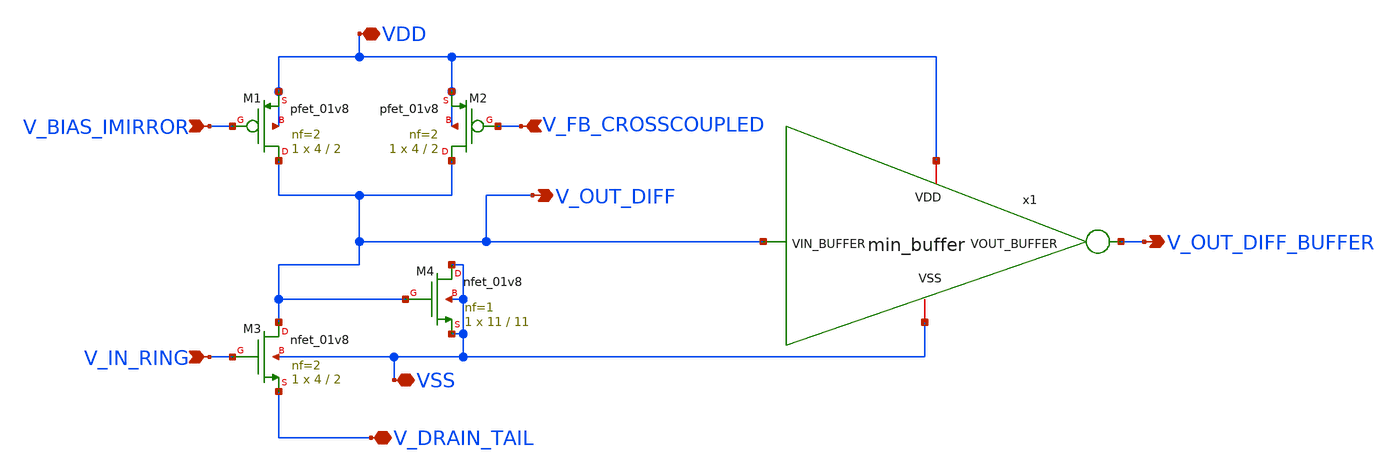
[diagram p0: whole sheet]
** sch_path: xschem/diff_stage_half.sch
**.subckt diff_stage_half V_BIAS_IMIRROR V_FB_CROSSCOUPLED V_IN_RING V_OUT_DIFF VDD VSS
*+ V_OUT_DIFF_BUFFER V_DRAIN_TAIL
*.ipin V_BIAS_IMIRROR
*.ipin V_FB_CROSSCOUPLED
*.ipin V_IN_RING
*.opin V_OUT_DIFF
*.iopin VDD
*.iopin VSS
*.opin V_OUT_DIFF_BUFFER
*.iopin V_DRAIN_TAIL
XM1 V_OUT_DIFF V_BIAS_IMIRROR VDD VDD sky130_fd_pr__pfet_01v8 L=2 W=4 nf=2 ad='int((nf+1)/2) * W/nf * 0.29'
+ as='int((nf+2)/2) * W/nf * 0.29' pd='2*int((nf+1)/2) * (W/nf + 0.29)' ps='2*int((nf+2)/2) * (W/nf + 0.29)'
+ nrd='0.29 / W' nrs='0.29 / W' sa=0 sb=0 sd=0 mult=1 m=1
XM2 V_OUT_DIFF V_FB_CROSSCOUPLED VDD VDD sky130_fd_pr__pfet_01v8 L=2 W=4 nf=2 ad='int((nf+1)/2) * W/nf * 0.29'
+ as='int((nf+2)/2) * W/nf * 0.29' pd='2*int((nf+1)/2) * (W/nf + 0.29)' ps='2*int((nf+2)/2) * (W/nf + 0.29)'
+ nrd='0.29 / W' nrs='0.29 / W' sa=0 sb=0 sd=0 mult=1 m=1
XM3 V_OUT_DIFF V_IN_RING V_DRAIN_TAIL VSS sky130_fd_pr__nfet_01v8 L=2 W=4 nf=2 ad='int((nf+1)/2) * W/nf * 0.29'
+ as='int((nf+2)/2) * W/nf * 0.29' pd='2*int((nf+1)/2) * (W/nf + 0.29)' ps='2*int((nf+2)/2) * (W/nf + 0.29)'
+ nrd='0.29 / W' nrs='0.29 / W' sa=0 sb=0 sd=0 mult=1 m=1
XM4 VSS V_OUT_DIFF VSS VSS sky130_fd_pr__nfet_01v8 L=11 W=11 nf=1 ad='int((nf+1)/2) * W/nf * 0.29' as='int((nf+2)/2) * W/nf * 0.29'
+ pd='2*int((nf+1)/2) * (W/nf + 0.29)' ps='2*int((nf+2)/2) * (W/nf + 0.29)' nrd='0.29 / W' nrs='0.29 / W'
+ sa=0 sb=0 sd=0 mult=1 m=1
x1 VDD VSS V_OUT_DIFF_BUFFER V_OUT_DIFF min_buffer
**.ends

* expanding   symbol:  min_buffer.sym # of pins=4
** sym_path: xschem/min_buffer.sym
** sch_path: xschem/min_buffer.sch
.subckt min_buffer VDD VSS VOUT_BUFFER VIN_BUFFER
*.ipin VIN_BUFFER
*.opin VOUT_BUFFER
*.iopin VDD
*.iopin VSS
x1 VDD VSS VOUT_BUFFER INT_BUFFER min_inv
x2 VDD VSS INT_BUFFER VIN_BUFFER min_inv
.ends


* expanding   symbol:  min_inv.sym # of pins=4
** sym_path: xschem/min_inv.sym
** sch_path: xschem/min_inv.sch
.subckt min_inv VDD VSS VOUT_INV VIN_INV
*.iopin VDD
*.iopin VSS
*.ipin VIN_INV
*.opin VOUT_INV
XM2 VOUT_INV VIN_INV VSS VSS sky130_fd_pr__nfet_01v8 L=0.15 W=1 nf=1 ad='int((nf+1)/2) * W/nf * 0.29'
+ as='int((nf+2)/2) * W/nf * 0.29' pd='2*int((nf+1)/2) * (W/nf + 0.29)' ps='2*int((nf+2)/2) * (W/nf + 0.29)'
+ nrd='0.29 / W' nrs='0.29 / W' sa=0 sb=0 sd=0 mult=1 m=1
XM3 VOUT_INV VIN_INV VDD VDD sky130_fd_pr__pfet_01v8 L=0.15 W=1 nf=1 ad='int((nf+1)/2) * W/nf * 0.29'
+ as='int((nf+2)/2) * W/nf * 0.29' pd='2*int((nf+1)/2) * (W/nf + 0.29)' ps='2*int((nf+2)/2) * (W/nf + 0.29)'
+ nrd='0.29 / W' nrs='0.29 / W' sa=0 sb=0 sd=0 mult=1 m=1
.ends

.end
